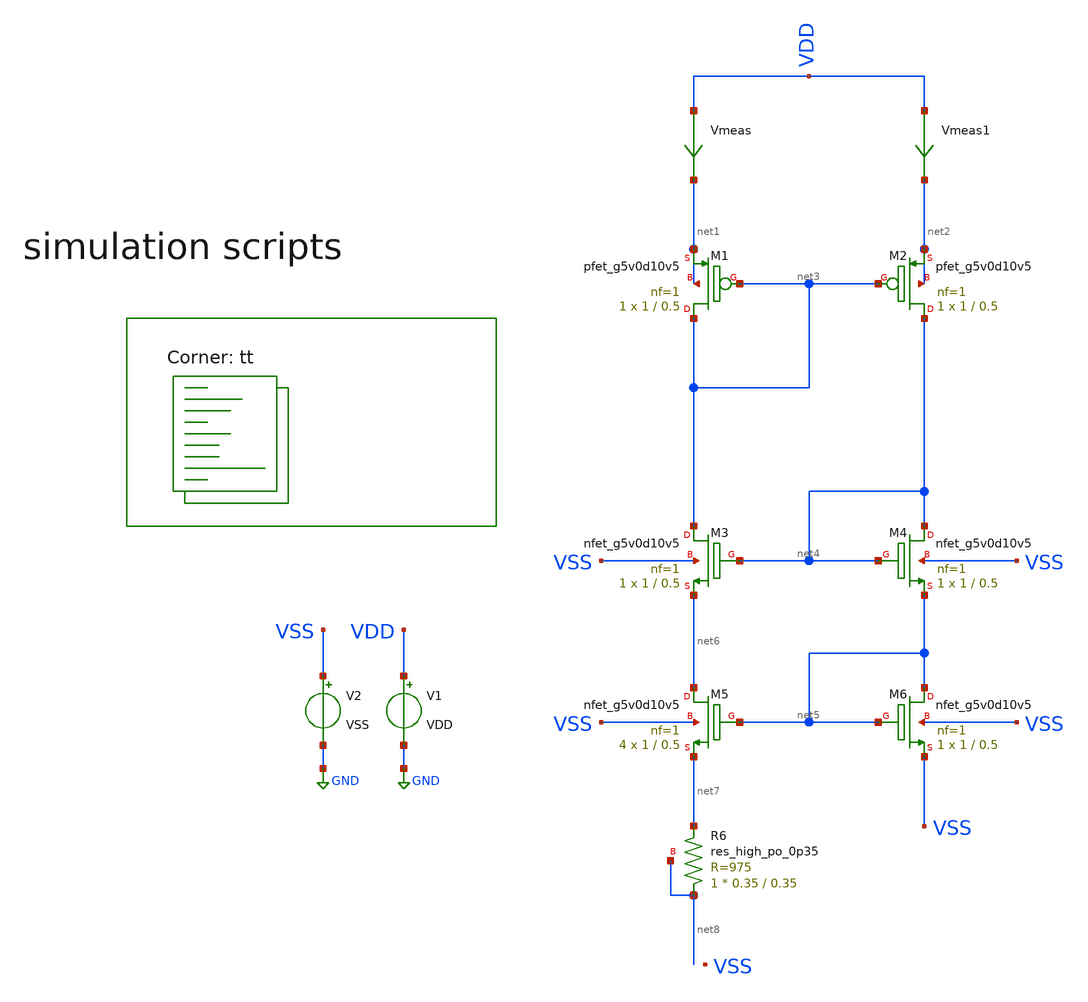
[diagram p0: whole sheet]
** sch_path: my_ip/testbenches_sky/transcondutance_cell/test.sch
**.subckt test
V1 VDD GND VDD
V2 VSS GND VSS
XM2 net4 net3 net2 net2 sky130_fd_pr__pfet_g5v0d10v5 L=0.5 W=1 nf=1 ad='int((1 + 1)/2) * 1 / 1 * 0.29'
+ as='int((1 + 2)/2) * 1 / 1 * 0.29' pd='2*int((1 + 1)/2) * (1 / 1 + 0.29)' ps='2*int((1 + 2)/2) * (1 / 1 + 0.29)'
+ nrd='0.29 / 1 ' nrs='0.29 / 1 ' sa=0 sb=0 sd=0 mult=1 m=1
XM1 net3 net3 net1 net1 sky130_fd_pr__pfet_g5v0d10v5 L=0.5 W=1 nf=1 ad='int((1 + 1)/2) * 1 / 1 * 0.29'
+ as='int((1 + 2)/2) * 1 / 1 * 0.29' pd='2*int((1 + 1)/2) * (1 / 1 + 0.29)' ps='2*int((1 + 2)/2) * (1 / 1 + 0.29)'
+ nrd='0.29 / 1 ' nrs='0.29 / 1 ' sa=0 sb=0 sd=0 mult=1 m=1
XM4 net4 net4 net5 VSS sky130_fd_pr__nfet_g5v0d10v5 L=0.5 W=1 nf=1 ad='int((1 + 1)/2) * 1 / 1 * 0.29'
+ as='int((1 + 2)/2) * 1 / 1 * 0.29' pd='2*int((1 + 1)/2) * (1 / 1 + 0.29)' ps='2*int((1 + 2)/2) * (1 / 1 + 0.29)'
+ nrd='0.29 / 1 ' nrs='0.29 / 1 ' sa=0 sb=0 sd=0 mult=1 m=1
XM3 net3 net4 net6 VSS sky130_fd_pr__nfet_g5v0d10v5 L=0.5 W=1 nf=1 ad='int((1 + 1)/2) * 1 / 1 * 0.29'
+ as='int((1 + 2)/2) * 1 / 1 * 0.29' pd='2*int((1 + 1)/2) * (1 / 1 + 0.29)' ps='2*int((1 + 2)/2) * (1 / 1 + 0.29)'
+ nrd='0.29 / 1 ' nrs='0.29 / 1 ' sa=0 sb=0 sd=0 mult=1 m=1
XM5 net6 net5 net7 VSS sky130_fd_pr__nfet_g5v0d10v5 L=0.5 W=1 nf=1 ad='int((1 + 1)/2) * 1 / 1 * 0.29'
+ as='int((1 + 2)/2) * 1 / 1 * 0.29' pd='2*int((1 + 1)/2) * (1 / 1 + 0.29)' ps='2*int((1 + 2)/2) * (1 / 1 + 0.29)'
+ nrd='0.29 / 1 ' nrs='0.29 / 1 ' sa=0 sb=0 sd=0 mult=4 m=4
XR6 net8 net7 net8 sky130_fd_pr__res_high_po_0p35 L=0.35 mult=1 m=1
Vmeas VDD net1 0
.save i(vmeas)
Vmeas1 VDD net2 0
.save i(vmeas1)
XM6 net5 net5 VSS VSS sky130_fd_pr__nfet_g5v0d10v5 L=0.5 W=1 nf=1 ad='int((1 + 1)/2) * 1 / 1 * 0.29'
+ as='int((1 + 2)/2) * 1 / 1 * 0.29' pd='2*int((1 + 1)/2) * (1 / 1 + 0.29)' ps='2*int((1 + 2)/2) * (1 / 1 + 0.29)'
+ nrd='0.29 / 1 ' nrs='0.29 / 1 ' sa=0 sb=0 sd=0 mult=1 m=1
**** begin user architecture code
.lib $::SKYWATER_MODELS/sky130.lib.spice tt


.Temp 27
.param VDD = 5
.param VSS = 0
.param VCM={(VDD-VSS)/2}
.param VCM_NEG={-VCM}
.param V_OFF = 0

.control
save all

dc Temp -40 125 1
plot i(Vmeas) i(Vmeas1)


.endc

**** end user architecture code
**.ends
.GLOBAL GND
.end
